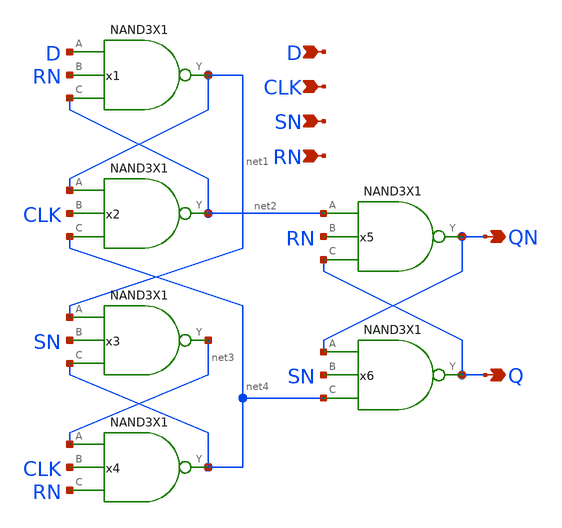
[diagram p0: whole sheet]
** sch_path: current/xschem/DFFSNRNX1.sch
**.subckt DFFSNRNX1 Q QN D CLK SN RN
*.opin Q
*.opin QN
*.ipin D
*.ipin CLK
*.ipin SN
*.ipin RN
x1 net1 D RN net2 VDD VSS NAND3X1
x2 net2 net1 CLK net4 VDD VSS NAND3X1
x3 net3 net1 SN net4 VDD VSS NAND3X1
x4 net4 net3 CLK RN VDD VSS NAND3X1
x5 QN net2 RN Q VDD VSS NAND3X1
x6 Q QN SN net4 VDD VSS NAND3X1
**.ends
.end
